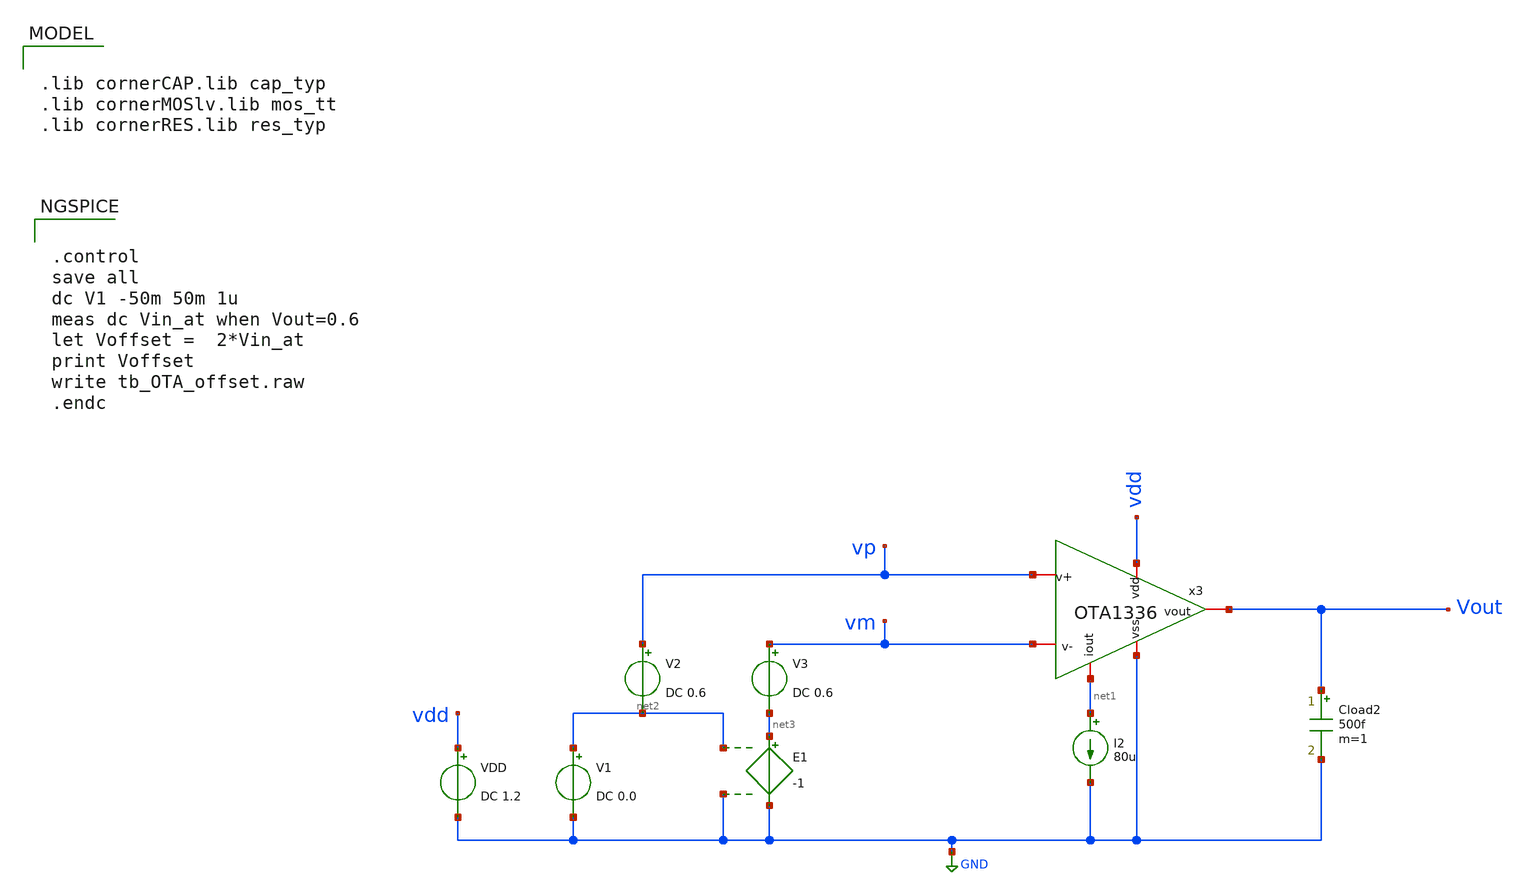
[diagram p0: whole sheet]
** sch_path: tests/data/OTA1336/testbenches/dc/xschem/OTA1336_offset.sch
**.subckt OTA1336_offset
VDD vdd GND DC 1.2
I2 net1 GND 80u
V1 net2 GND DC 0.0
x3 vdd net1 Vout vm vp GND OTA1336
Cload2 Vout GND 500f m=1
V2 vp net2 DC 0.6
V3 vm net3 DC 0.6
E1 net3 GND net2 GND -1
**** begin user architecture code

.lib cornerCAP.lib cap_typ
.lib cornerMOSlv.lib mos_tt
.lib cornerRES.lib res_typ




.control
save all
dc V1 -50m 50m 1u
meas dc Vin_at when Vout=0.6
let Voffset =  2*Vin_at
print Voffset
write tb_OTA_offset.raw
.endc


**** end user architecture code
**.ends
.GLOBAL GND
.end
